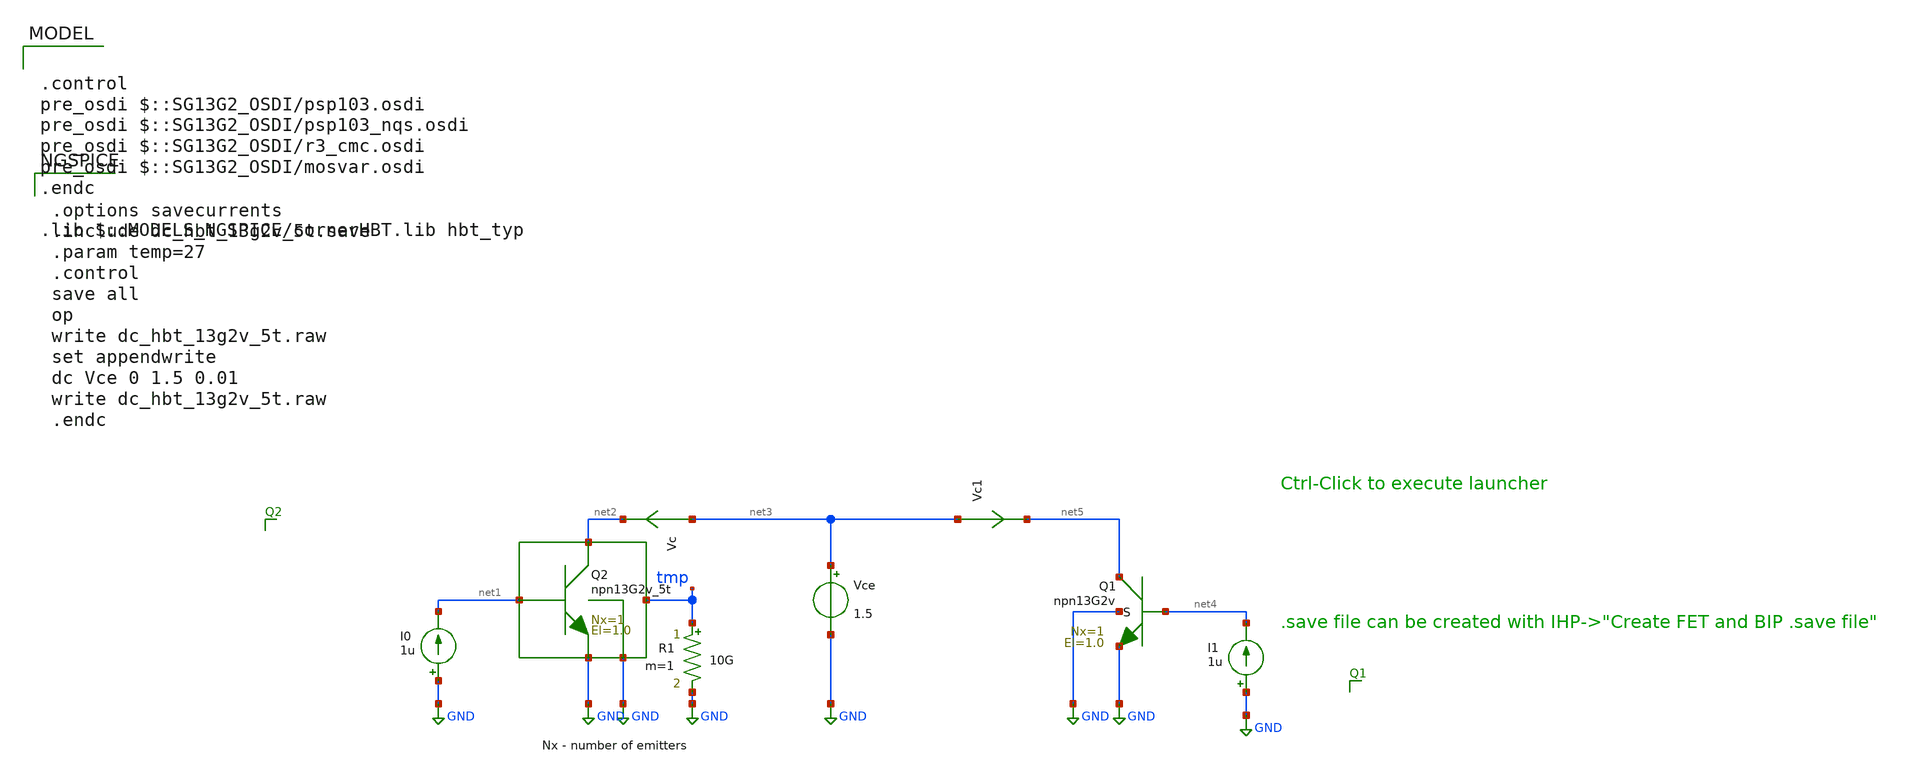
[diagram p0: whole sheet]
** sch_path: ihp-sg13g2/xschem_libs/sg13g2_tests/dc_hbt_13g2v_5t/schematic/dc_hbt_13g2v_5t.sch
* Copyright 2023 IHP PDK Authors
**.subckt dc_hbt_13g2v_5t
Vce net3 GND 1.5
I0 GND net1 1u
Vc net3 net2 0
.save i(vc)
R1 tmp GND 10G m=1
I1 GND net4 1u
Vc1 net3 net5 0
.save i(vc1)
XQ1 net5 net4 GND GND npn13G2v Nx=1 El=1.0 mm_ok=1
XQ2 net2 net1 GND GND tmp npn13G2v_5t Nx=1 El=1.0 mm_ok=1
**** begin user architecture code


.options savecurrents
.include dc_hbt_13g2v_5t.save
.param temp=27
.control
save all
op
write dc_hbt_13g2v_5t.raw
set appendwrite
dc Vce 0 1.5 0.01
write dc_hbt_13g2v_5t.raw
.endc



.control
pre_osdi $::SG13G2_OSDI/psp103.osdi
pre_osdi $::SG13G2_OSDI/psp103_nqs.osdi
pre_osdi $::SG13G2_OSDI/r3_cmc.osdi
pre_osdi $::SG13G2_OSDI/mosvar.osdi
.endc

.lib $::MODELS_NGSPICE/cornerHBT.lib hbt_typ

**** end user architecture code
**.ends
.GLOBAL GND
.end
